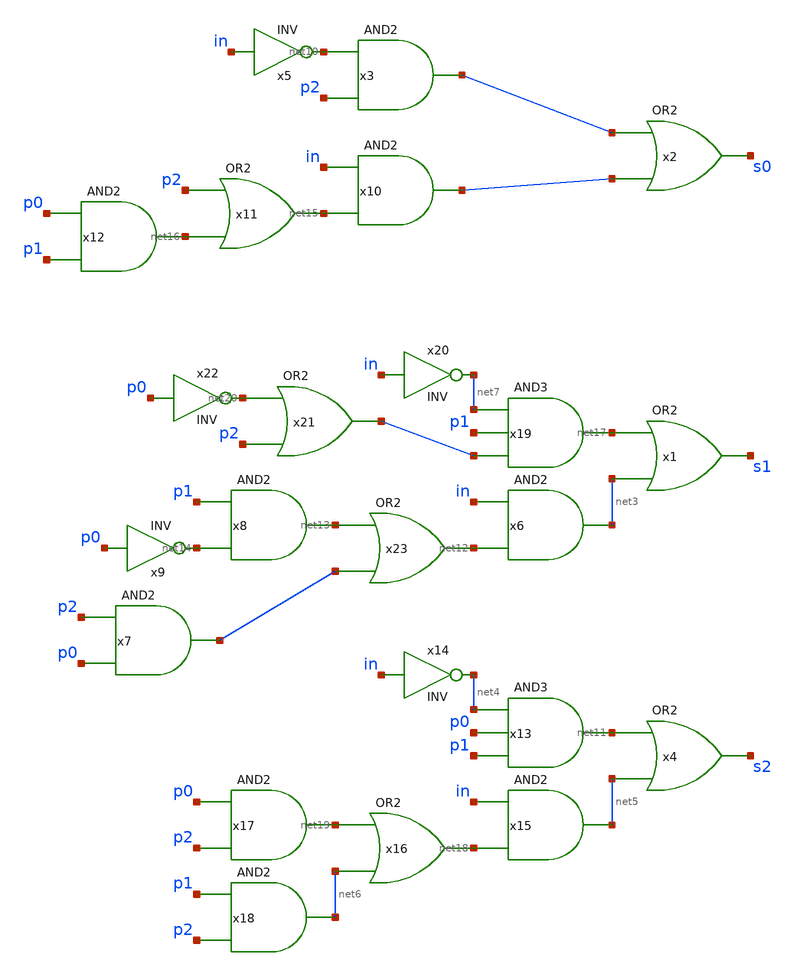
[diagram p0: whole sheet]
** sch_path: 1bit_adc/logic_gates_three_bit_adc.sch
**.subckt logic_gates_three_bit_adc
x2 s0 net1 net2 VCC VSS VCC VSS OR2
x3 net1 net10 p2 VCC VSS VCC VSS AND2
x4 s2 net11 net5 VCC VSS VCC VSS OR2
x5 net10 in VCC VSS VCC VSS INV
x6 net3 in net12 VCC VSS VCC VSS AND2
x7 net9 p2 p0 VCC VSS VCC VSS AND2
x8 net13 p1 net14 VCC VSS VCC VSS AND2
x9 net14 p0 VCC VSS VCC VSS INV
x10 net2 in net15 VCC VSS VCC VSS AND2
x11 net15 p2 net16 VCC VSS VCC VSS OR2
x12 net16 p0 p1 VCC VSS VCC VSS AND2
x1 s1 net17 net3 VCC VSS VCC VSS OR2
x13 net11 net4 p0 p1 VCC VSS VCC VSS AND3
x14 net4 in VCC VSS VCC VSS INV
x15 net5 in net18 VCC VSS VCC VSS AND2
x16 net18 net19 net6 VCC VSS VCC VSS OR2
x17 net19 p0 p2 VCC VSS VCC VSS AND2
x18 net6 p1 p2 VCC VSS VCC VSS AND2
x19 net17 net7 p1 net8 VCC VSS VCC VSS AND3
x20 net7 in VCC VSS VCC VSS INV
x21 net8 net20 p2 VCC VSS VCC VSS OR2
x22 net20 p0 VCC VSS VCC VSS INV
x23 net12 net13 net9 VCC VSS VCC VSS OR2
**.ends
.end
